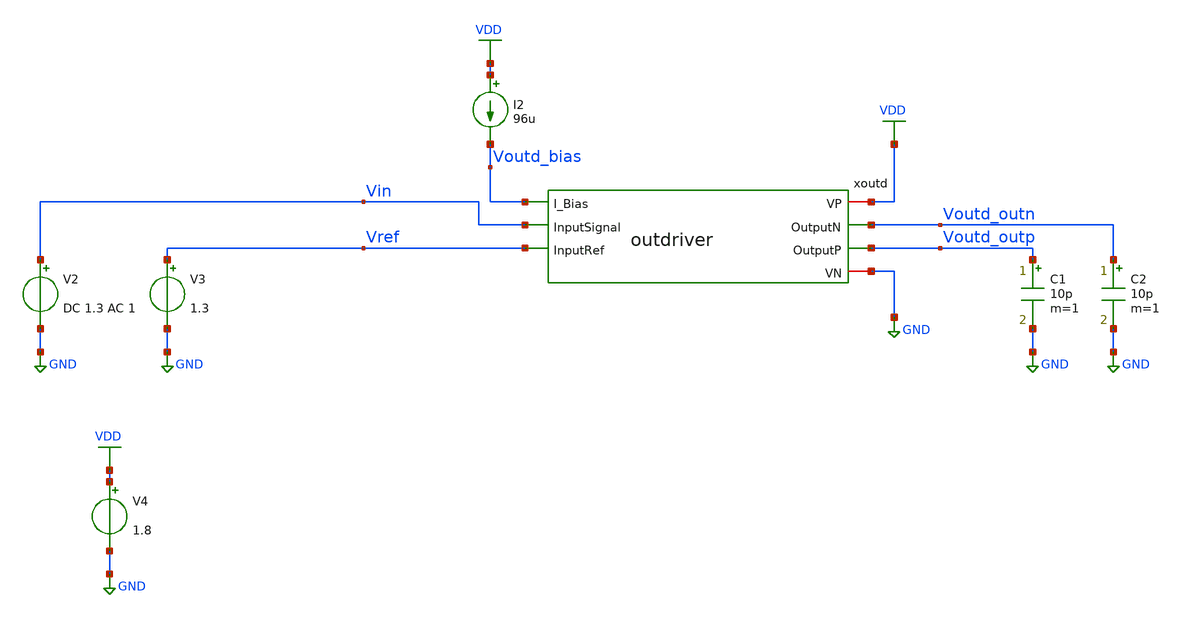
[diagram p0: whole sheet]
** sch_path: xschem/test/test_outd.sch
**.subckt test_outd
I2 VDD Voutd_bias 96u
V2 Vin GND DC 1.3 AC 1
V3 Vref GND 1.3
V4 VDD GND 1.8
xoutd VDD Voutd_outn Voutd_outp Voutd_bias Vin Vref GND outdriver
C1 Voutd_outp GND 10p m=1
C2 Voutd_outn GND 10p m=1
**** begin user architecture code


*.options savecurrents
.option warn=1
.control
set wr_vecnames
set wr_singlescale
set hcopydevtype=svg

reset

op
save currents
write test_outd.raw
run
reset

ac dec 10 1 1T
plot db(v(voutd_outp)-v(voutd_outn))
plot db(v(xoutd.V_da2_P)-v(xoutd.V_da2_N))
plot db(v(xoutd.V_da1_P)-v(xoutd.V_da1_N))

* hardcopy filter_gain.svg db(v(Vfilt1_N)-v(Vfilt1_P))
* noise v(voutd_outp) v2 dec 1000 2MEG 2G
* print all
* * wrdata result_noise.csv inoise_total onoise_total
* setplot noise1
* plot inoise_spectrum
* plot onoise_spectrum

reset
* noise v(xoutd.v_da1_p) v2 dec 1000 2MEG 2G
* setplot noise1
* plot inoise_spectrum
* plot onoise_spectrum
* run

* noise v(xoutd.v_da1_p) v2 dec 1000 10 1T
* print all
* setplot noise3
* plot inoise_spectrum
* plot onoise_spectrum
* run

* noise v(V_da2_P) v2 dec 1000 2MEG 2G
* setplot noise5
* plot inoise_spectrum
* plot onoise_spectrum
* run


noise v(voutd_outp) v2 dec 100 10 1T
print all
setplot noise1
plot inoise_spectrum
plot onoise_spectrum
run

noise v(voutd_outp) v2 dec 100 1MEG 10G
print all
setplot noise3
plot inoise_spectrum
plot onoise_spectrum
run




* noise v(V_da2_P) v2 dec 1000 10 1T
* print all
* setplot noise11
* plot inoise_spectrum
* plot onoise_spectrum
* run



.endc




* .include ../../tia.spice
* .include ../../filter_diff.spice
* .include ../../cmm_sense3.spice

* .include tia.spice
* .include filter_diff.spice
* .include diffamp.spice
* .include cmm_sense3.spice
* .include comp.spice
.include outdriver.spice



* .lib $::SKYWATER_MODELS/sky130.lib.spice #model#
.lib $::SKYWATER_MODELS/sky130.lib.spice.tt.red tt
* .lib /home/simon/share/pdk/sky130A/libs.tech/ngspice/sky130.lib.spice.tt.red tt

**** end user architecture code
**.ends

* expanding   symbol:  /home/simon/code/asic/analog/outdriver/outdriver.sym # of pins=7
** sym_path: xschem/outdriver/outdriver.sym
** sch_path: xschem/outdriver/outdriver.sch
.subckt outdriver VP OutputN OutputP I_Bias InputSignal InputRef VN
*.iopin VN
*.ipin InputRef
*.iopin VP
*.ipin I_Bias
*.ipin InputSignal
*.opin OutputN
*.opin OutputP
XM1 V_da1_P InputSignal VM6D VM6D sky130_fd_pr__nfet_01v8_lvt L=0.15 W=2 nf=1 ad='int((nf+1)/2) * W/nf * 0.29'
+ as='int((nf+2)/2) * W/nf * 0.29' pd='2*int((nf+1)/2) * (W/nf + 0.29)' ps='2*int((nf+2)/2) * (W/nf + 0.29)'
+ nrd='0.29 / W' nrs='0.29 / W' sa=0 sb=0 sd=0 mult=11*2 m=11*2
XM3 VM3D I_Bias net4 VN sky130_fd_pr__nfet_01v8 L=0.5 W=2 nf=1 ad='int((nf+1)/2) * W/nf * 0.29' as='int((nf+2)/2) * W/nf * 0.29'
+ pd='2*int((nf+1)/2) * (W/nf + 0.29)' ps='2*int((nf+2)/2) * (W/nf + 0.29)' nrd='0.29 / W' nrs='0.29 / W'
+ sa=0 sb=0 sd=0 mult=2*(64) m=2*(64)
XM6 VM6D I_Bias VM3D VN sky130_fd_pr__nfet_01v8 L=0.15 W=2 nf=1 ad='int((nf+1)/2) * W/nf * 0.29' as='int((nf+2)/2) * W/nf * 0.29'
+ pd='2*int((nf+1)/2) * (W/nf + 0.29)' ps='2*int((nf+2)/2) * (W/nf + 0.29)' nrd='0.29 / W' nrs='0.29 / W'
+ sa=0 sb=0 sd=0 mult=64 m=64
XM7 I_Bias I_Bias net1 VN sky130_fd_pr__nfet_01v8 L=0.15 W=2 nf=1 ad='int((nf+1)/2) * W/nf * 0.29' as='int((nf+2)/2) * W/nf * 0.29'
+ pd='2*int((nf+1)/2) * (W/nf + 0.29)' ps='2*int((nf+2)/2) * (W/nf + 0.29)' nrd='0.29 / W' nrs='0.29 / W'
+ sa=0 sb=0 sd=0 mult=2 m=2
XM8 net1 I_Bias VN VN sky130_fd_pr__nfet_01v8 L=0.5 W=2 nf=1 ad='int((nf+1)/2) * W/nf * 0.29' as='int((nf+2)/2) * W/nf * 0.29'
+ pd='2*int((nf+1)/2) * (W/nf + 0.29)' ps='2*int((nf+2)/2) * (W/nf + 0.29)' nrd='0.29 / W' nrs='0.29 / W'
+ sa=0 sb=0 sd=0 mult=2*2 m=2*2
XM2 V_da2_P V_da1_P VM1_D VM1_D sky130_fd_pr__nfet_01v8_lvt L=0.15 W=2 nf=1 ad='int((nf+1)/2) * W/nf * 0.29'
+ as='int((nf+2)/2) * W/nf * 0.29' pd='2*int((nf+1)/2) * (W/nf + 0.29)' ps='2*int((nf+2)/2) * (W/nf + 0.29)'
+ nrd='0.29 / W' nrs='0.29 / W' sa=0 sb=0 sd=0 mult=44*2 m=44*2
XM4 V_da2_N V_da1_N VM1_D VM1_D sky130_fd_pr__nfet_01v8_lvt L=0.15 W=2 nf=1 ad='int((nf+1)/2) * W/nf * 0.29'
+ as='int((nf+2)/2) * W/nf * 0.29' pd='2*int((nf+1)/2) * (W/nf + 0.29)' ps='2*int((nf+2)/2) * (W/nf + 0.29)'
+ nrd='0.29 / W' nrs='0.29 / W' sa=0 sb=0 sd=0 mult=44*2 m=44*2
XM9 net2 I_Bias net5 VN sky130_fd_pr__nfet_01v8 L=0.5 W=2 nf=1 ad='int((nf+1)/2) * W/nf * 0.29' as='int((nf+2)/2) * W/nf * 0.29'
+ pd='2*int((nf+1)/2) * (W/nf + 0.29)' ps='2*int((nf+2)/2) * (W/nf + 0.29)' nrd='0.29 / W' nrs='0.29 / W'
+ sa=0 sb=0 sd=0 mult=2*(256+64) m=2*(256+64)
XM10 VM1_D I_Bias net2 VN sky130_fd_pr__nfet_01v8 L=0.15 W=2 nf=1 ad='int((nf+1)/2) * W/nf * 0.29' as='int((nf+2)/2) * W/nf * 0.29'
+ pd='2*int((nf+1)/2) * (W/nf + 0.29)' ps='2*int((nf+2)/2) * (W/nf + 0.29)' nrd='0.29 / W' nrs='0.29 / W'
+ sa=0 sb=0 sd=0 mult=256+64 m=256+64
XM11 OutputP V_da2_P VM14D VM14D sky130_fd_pr__nfet_01v8_lvt L=0.15 W=2 nf=1 ad='int((nf+1)/2) * W/nf * 0.29'
+ as='int((nf+2)/2) * W/nf * 0.29' pd='2*int((nf+1)/2) * (W/nf + 0.29)' ps='2*int((nf+2)/2) * (W/nf + 0.29)'
+ nrd='0.29 / W' nrs='0.29 / W' sa=0 sb=0 sd=0 mult=44*4*2 m=44*4*2
XM12 OutputN V_da2_N VM14D VM14D sky130_fd_pr__nfet_01v8_lvt L=0.15 W=2 nf=1 ad='int((nf+1)/2) * W/nf * 0.29'
+ as='int((nf+2)/2) * W/nf * 0.29' pd='2*int((nf+1)/2) * (W/nf + 0.29)' ps='2*int((nf+2)/2) * (W/nf + 0.29)'
+ nrd='0.29 / W' nrs='0.29 / W' sa=0 sb=0 sd=0 mult=44*4*2 m=44*4*2
XM13 net3 I_Bias net6 VN sky130_fd_pr__nfet_01v8 L=0.5 W=2 nf=1 ad='int((nf+1)/2) * W/nf * 0.29' as='int((nf+2)/2) * W/nf * 0.29'
+ pd='2*int((nf+1)/2) * (W/nf + 0.29)' ps='2*int((nf+2)/2) * (W/nf + 0.29)' nrd='0.29 / W' nrs='0.29 / W'
+ sa=0 sb=0 sd=0 mult=2*(1024+256) m=2*(1024+256)
XM14 VM14D I_Bias net3 VN sky130_fd_pr__nfet_01v8 L=0.15 W=2 nf=1 ad='int((nf+1)/2) * W/nf * 0.29' as='int((nf+2)/2) * W/nf * 0.29'
+ pd='2*int((nf+1)/2) * (W/nf + 0.29)' ps='2*int((nf+2)/2) * (W/nf + 0.29)' nrd='0.29 / W' nrs='0.29 / W'
+ sa=0 sb=0 sd=0 mult=1024+256 m=1024+256
XR7 V_da2_N VP VP sky130_fd_pr__res_high_po_5p73 L=4 mult=4*2 m=4*2
XR5 V_da2_P VP VP sky130_fd_pr__res_high_po_5p73 L=4 mult=4*2 m=4*2
XR3 V_da1_N VP VP sky130_fd_pr__res_high_po_2p85 L=6 mult=4 m=4
XR4 V_da1_P VP VP sky130_fd_pr__res_high_po_2p85 L=6 mult=4 m=4
XC2 InputRef VN sky130_fd_pr__cap_mim_m3_2 W=30 L=30 MF=1 m=1
XM5 V_da1_N InputRef VM6D VM6D sky130_fd_pr__nfet_01v8_lvt L=0.15 W=2 nf=1 ad='int((nf+1)/2) * W/nf * 0.29'
+ as='int((nf+2)/2) * W/nf * 0.29' pd='2*int((nf+1)/2) * (W/nf + 0.29)' ps='2*int((nf+2)/2) * (W/nf + 0.29)'
+ nrd='0.29 / W' nrs='0.29 / W' sa=0 sb=0 sd=0 mult=11*2 m=11*2
XR8 OutputP VP VP sky130_fd_pr__res_high_po_5p73 L=4 mult=16*2 m=16*2
XC1 InputRef VN sky130_fd_pr__cap_mim_m3_2 W=30 L=30 MF=1 m=1
XC6 VP VN sky130_fd_pr__cap_mim_m3_2 W=30 L=30 MF=1 m=1
XC8 VP VN sky130_fd_pr__cap_mim_m3_2 W=30 L=30 MF=1 m=1
V1 net4 VN 0
V2 net5 VN 0
V3 net6 VN 0
XR1 OutputN VP VP sky130_fd_pr__res_high_po_5p73 L=4 mult=16*2 m=16*2
XC7 VP VN sky130_fd_pr__cap_mim_m3_2 W=30 L=30 MF=1 m=1
XC9 VP VN sky130_fd_pr__cap_mim_m3_2 W=30 L=30 MF=1 m=1
XC10 VP VN sky130_fd_pr__cap_mim_m3_2 W=30 L=30 MF=1 m=1
XC11 VP VN sky130_fd_pr__cap_mim_m3_2 W=30 L=30 MF=1 m=1
XC12 VP VN sky130_fd_pr__cap_mim_m3_2 W=30 L=30 MF=1 m=1
XC13 VP VN sky130_fd_pr__cap_mim_m3_2 W=30 L=30 MF=1 m=1
XC14 VP VN sky130_fd_pr__cap_mim_m3_2 W=30 L=30 MF=1 m=1
XC5 I_Bias VN sky130_fd_pr__cap_mim_m3_1 W=20 L=20 MF=1 m=1
XC3 I_Bias VN sky130_fd_pr__cap_mim_m3_1 W=20 L=20 MF=1 m=1
.ends

.GLOBAL GND
.GLOBAL VDD
.end
